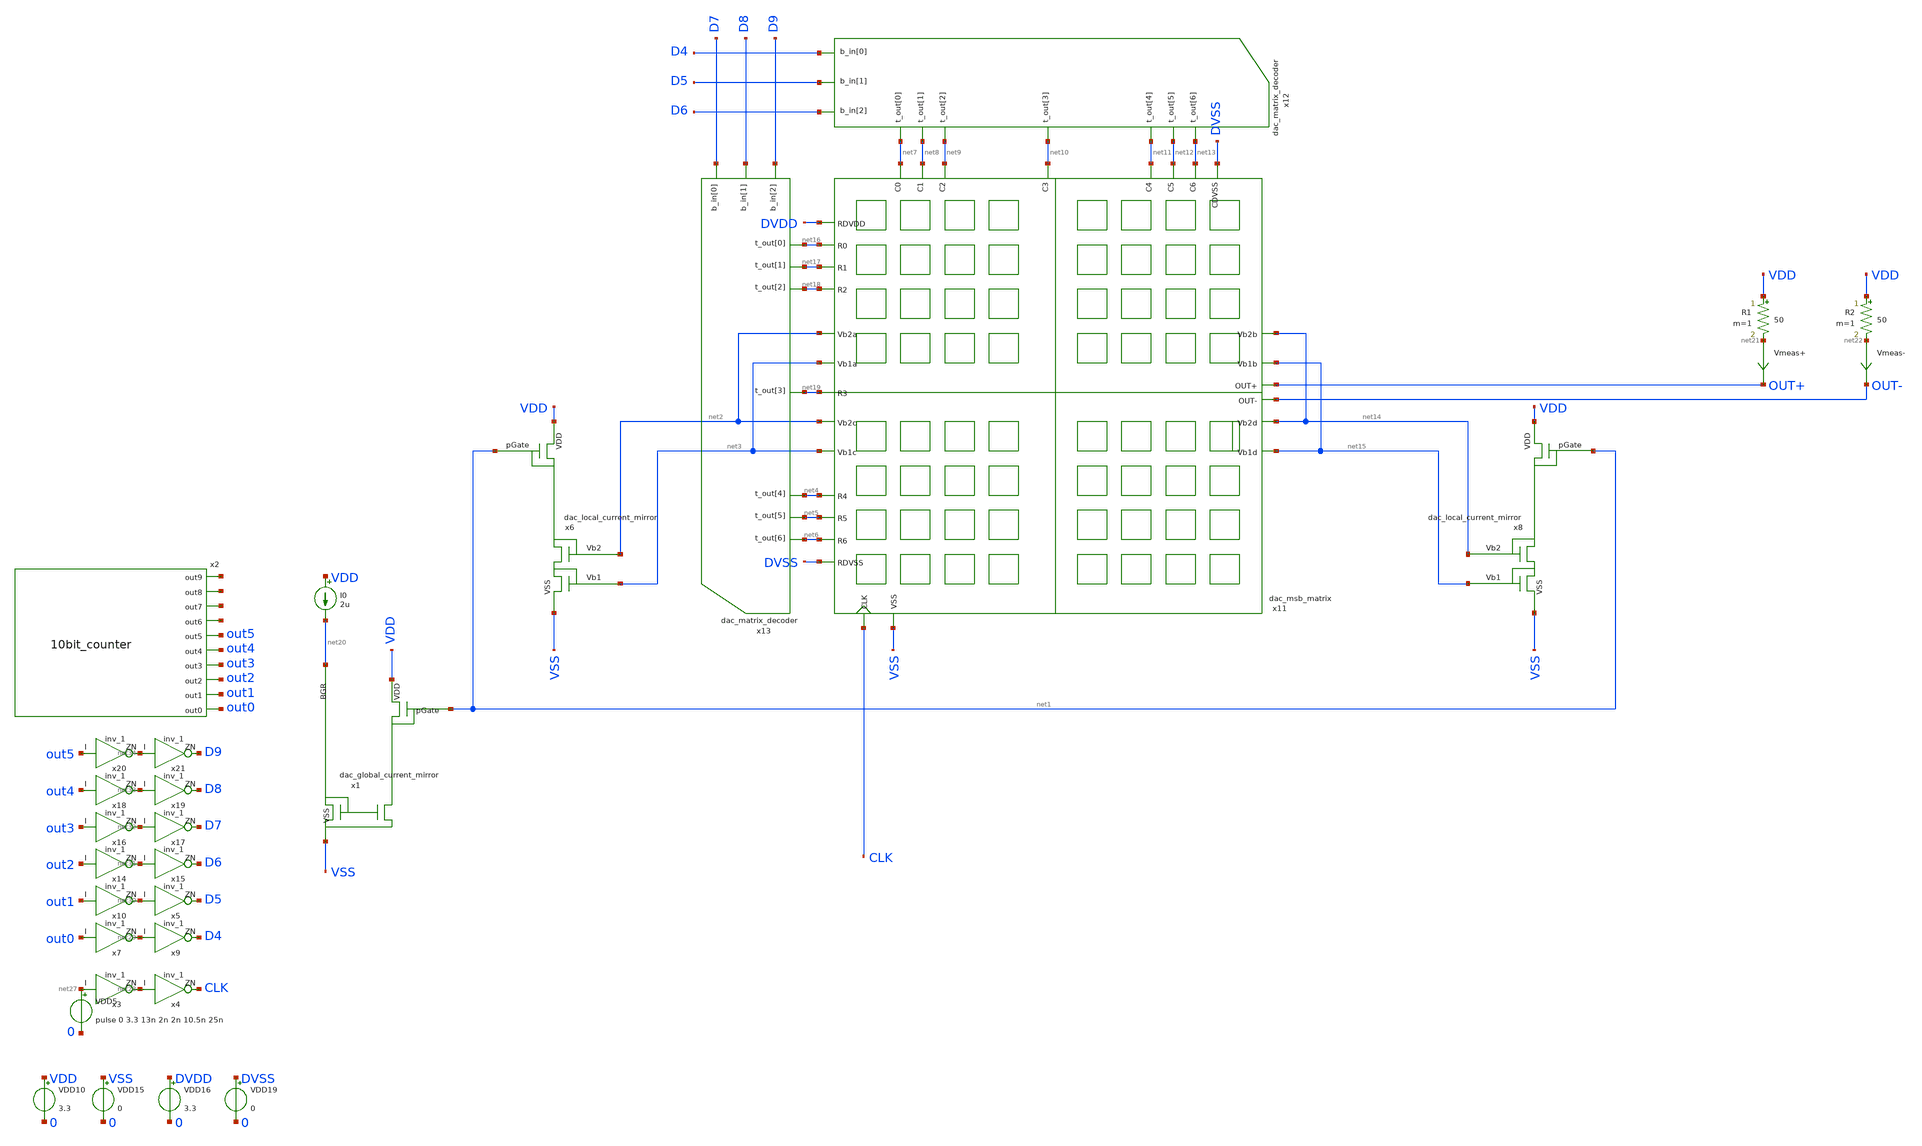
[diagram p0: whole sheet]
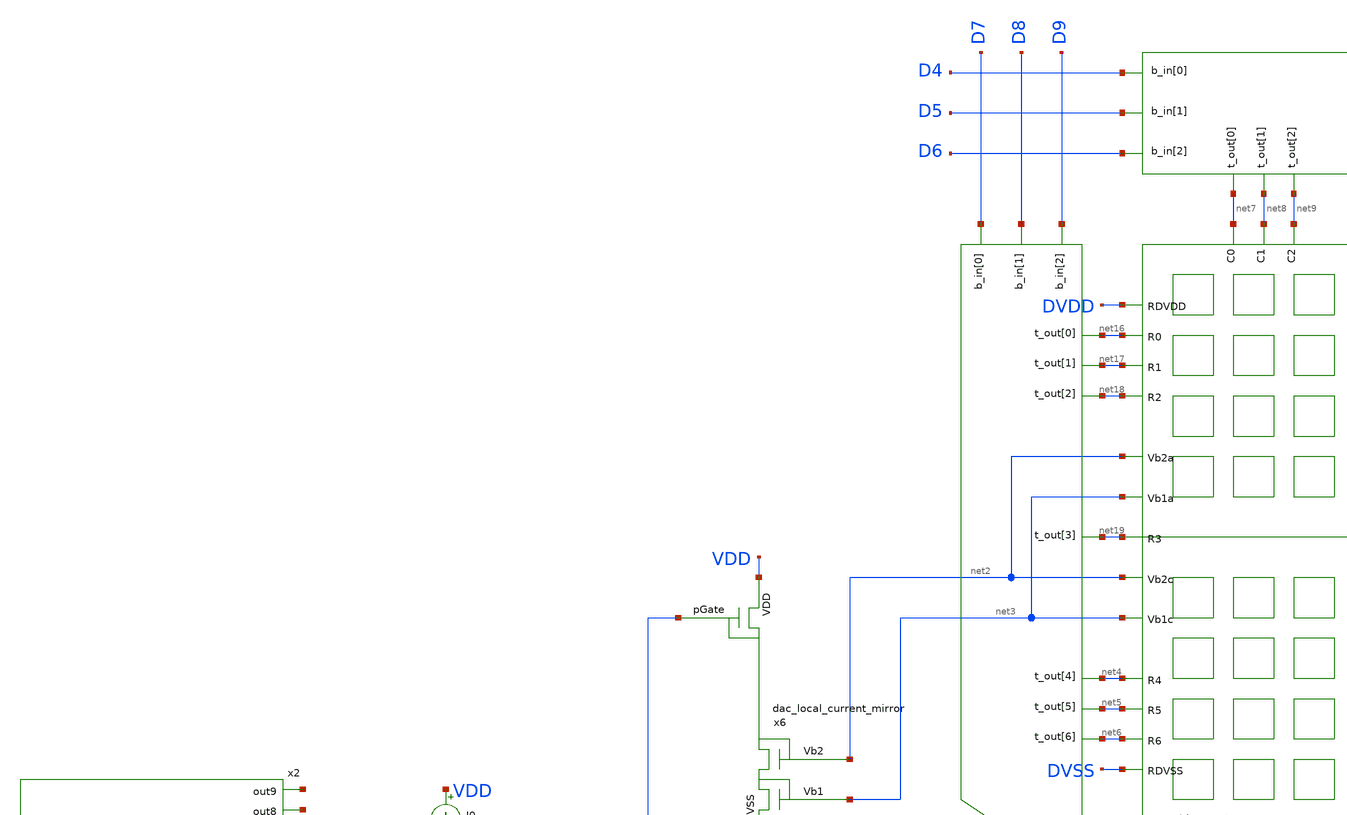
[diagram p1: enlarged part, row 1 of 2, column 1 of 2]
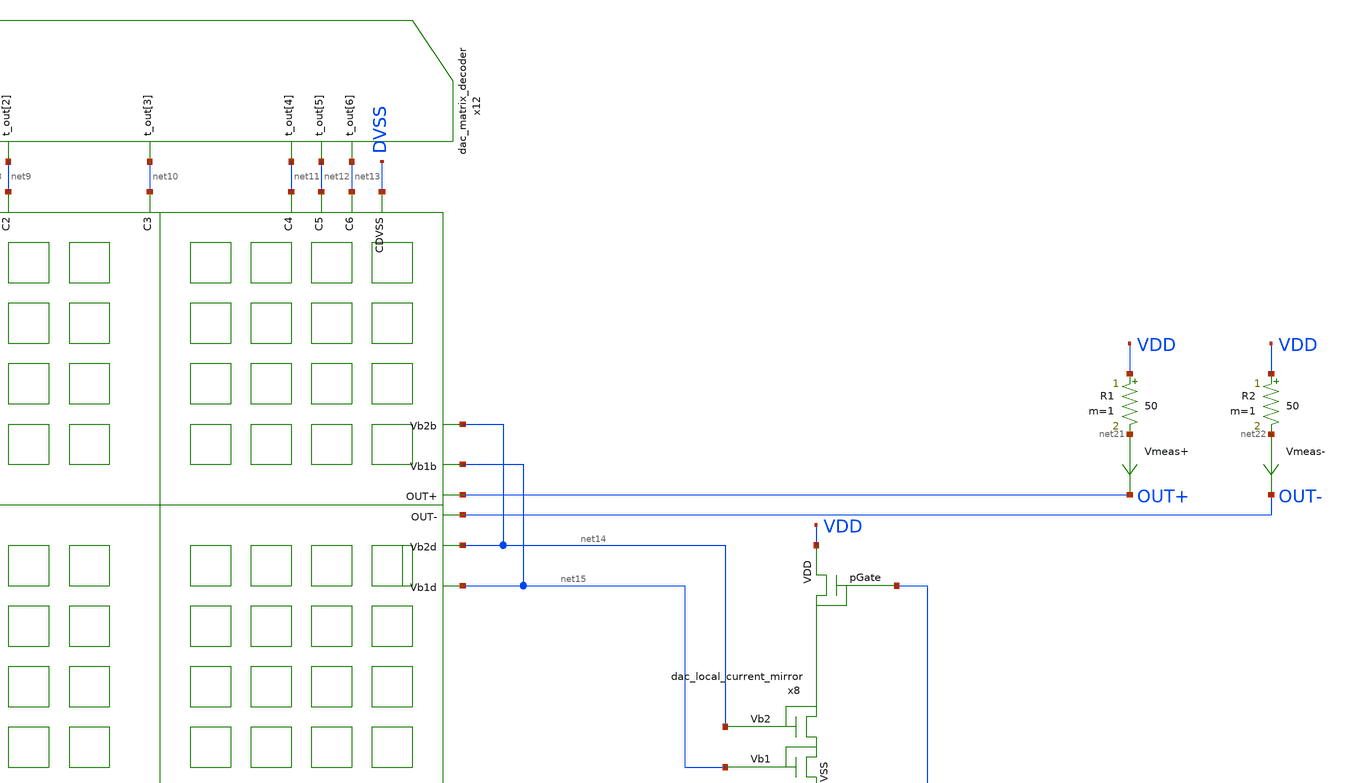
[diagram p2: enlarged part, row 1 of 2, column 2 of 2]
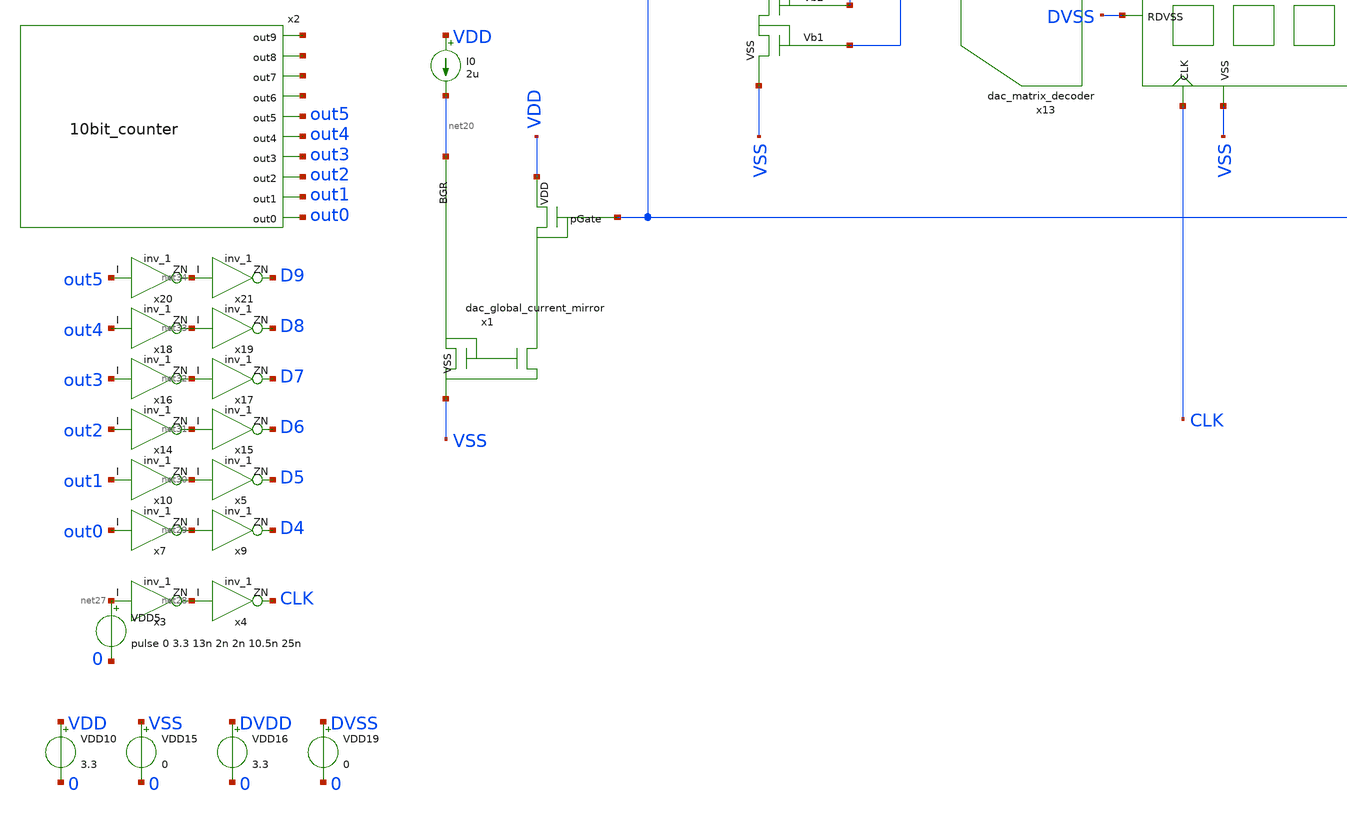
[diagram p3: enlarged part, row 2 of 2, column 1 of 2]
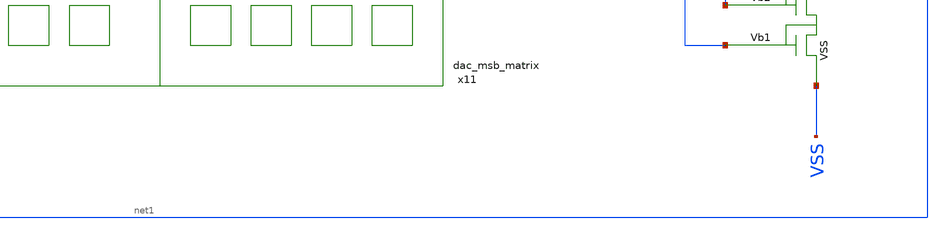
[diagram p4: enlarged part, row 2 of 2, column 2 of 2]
** sch_path: DAC/xschem/tb/tb_dac_msb_matrix.sch
**.subckt tb_dac_msb_matrix
VDD10 VDD 0 3.3
VDD15 VSS 0 0
VDD16 DVDD 0 3.3
VDD19 DVSS 0 0
I0 VDD net20 2u
R1 VDD net21 50 m=1
R2 VDD net22 50 m=1
Vmeas+ net21 OUT+ 0
.save i(vmeas+)
Vmeas- net22 OUT- 0
.save i(vmeas-)
x1 VDD net1 net20 VSS dac_global_current_mirror
x6 VDD net1 net2 net3 VSS dac_local_current_mirror
x8 VDD net1 net14 net15 VSS dac_local_current_mirror
x11 DVDD net16 net17 net18 net19 net4 net5 net6 DVSS net7 net8 net9 net10 net11 net12 net13 DVSS
+ net2 net3 net2 net3 net14 net15 net14 net15 CLK VSS OUT+ OUT- DVDD DVSS dac_msb_matrix
x12 D4 D5 D6 net7 net8 net9 net10 net11 net12 net13 DVDD DVSS dac_matrix_decoder
x13 D7 D8 D9 net16 net17 net18 net19 net4 net5 net6 DVDD DVSS dac_matrix_decoder
x2 out0 out1 out2 out3 out4 out5 net23 net24 net25 net26 10bit_counter
VDD5 net27 0 pulse 0 3.3 13n 2n 2n 10.5n 25n
x3 net27 net28 DVDD DVDD DVSS DVSS gf180mcu_fd_sc_mcu7t5v0__inv_1
x4 net28 CLK DVDD DVDD DVSS DVSS gf180mcu_fd_sc_mcu7t5v0__inv_1
x7 out0 net29 DVDD DVDD DVSS DVSS gf180mcu_fd_sc_mcu7t5v0__inv_1
x9 net29 D4 DVDD DVDD DVSS DVSS gf180mcu_fd_sc_mcu7t5v0__inv_1
x10 out1 net30 DVDD DVDD DVSS DVSS gf180mcu_fd_sc_mcu7t5v0__inv_1
x5 net30 D5 DVDD DVDD DVSS DVSS gf180mcu_fd_sc_mcu7t5v0__inv_1
x14 out2 net31 DVDD DVDD DVSS DVSS gf180mcu_fd_sc_mcu7t5v0__inv_1
x15 net31 D6 DVDD DVDD DVSS DVSS gf180mcu_fd_sc_mcu7t5v0__inv_1
x16 out3 net32 DVDD DVDD DVSS DVSS gf180mcu_fd_sc_mcu7t5v0__inv_1
x17 net32 D7 DVDD DVDD DVSS DVSS gf180mcu_fd_sc_mcu7t5v0__inv_1
x18 out4 net33 DVDD DVDD DVSS DVSS gf180mcu_fd_sc_mcu7t5v0__inv_1
x19 net33 D8 DVDD DVDD DVSS DVSS gf180mcu_fd_sc_mcu7t5v0__inv_1
x20 out5 net34 DVDD DVDD DVSS DVSS gf180mcu_fd_sc_mcu7t5v0__inv_1
x21 net34 D9 DVDD DVDD DVSS DVSS gf180mcu_fd_sc_mcu7t5v0__inv_1
**** begin user architecture code



.control
    tran 1n 1650n
    plot i(Vmeas+) i(Vmeas-)
    write test_dac_msb_matrix.raw
.endc
.save all




.include /home/junbeom/pico/designs/xschem/dac_matrix_decoder.spice
.include $::180MCU_MODELS/design.ngspice
.lib $::180MCU_MODELS/sm141064.ngspice typical
.lib $::180MCU_MODELS/sm141064.ngspice res_typical
.lib $::180MCU_MODELS/sm141064.ngspice moscap_typical
.include $::180MCU_STDCELLS/spice/gf180mcu_fd_sc_mcu7t5v0.spice
*.lib $::180MCU_MODELS/sm141064.ngspice res_statistical

**** end user architecture code
**.ends

* expanding   symbol:  dac_global_current_mirror.sym # of pins=4
** sym_path: DAC/xschem/dac_global_current_mirror.sym
** sch_path: DAC/xschem/dac_global_current_mirror.sch
.subckt dac_global_current_mirror VDD pGate BGR VSS
*.ipin BGR
*.ipin VDD
*.opin pGate
*.ipin VSS
XM1 pGate pGate VDD VDD pfet_03v3 L=1u W=1u nf=1 ad='int((nf+1)/2) * W/nf * 0.18u' as='int((nf+2)/2) * W/nf * 0.18u'
+ pd='2*int((nf+1)/2) * (W/nf + 0.18u)' ps='2*int((nf+2)/2) * (W/nf + 0.18u)' nrd='0.18u / W' nrs='0.18u / W'
+ sa=0 sb=0 sd=0 m=1
XMN1 BGR BGR VSS VSS nfet_03v3 L=4u W=1u nf=4 ad='int((nf+1)/2) * W/nf * 0.18u' as='int((nf+2)/2) * W/nf * 0.18u'
+ pd='2*int((nf+1)/2) * (W/nf + 0.18u)' ps='2*int((nf+2)/2) * (W/nf + 0.18u)' nrd='0.18u / W' nrs='0.18u / W'
+ sa=0 sb=0 sd=0 m=1
XMN2 pGate BGR VSS VSS nfet_03v3 L=4u W=1u nf=4 ad='int((nf+1)/2) * W/nf * 0.18u' as='int((nf+2)/2) * W/nf * 0.18u'
+ pd='2*int((nf+1)/2) * (W/nf + 0.18u)' ps='2*int((nf+2)/2) * (W/nf + 0.18u)' nrd='0.18u / W' nrs='0.18u / W'
+ sa=0 sb=0 sd=0 m=1
.ends


* expanding   symbol:  dac_local_current_mirror.sym # of pins=5
** sym_path: DAC/xschem/dac_local_current_mirror.sym
** sch_path: DAC/xschem/dac_local_current_mirror.sch
.subckt dac_local_current_mirror VDD pGate Vb2 Vb1 VSS
*.ipin VSS
*.opin Vb2
*.opin Vb1
*.ipin VDD
*.ipin pGate
XM2 Vb2 pGate VDD VDD pfet_03v3 L=1u W=5u nf=5 ad='int((nf+1)/2) * W/nf * 0.18u' as='int((nf+2)/2) * W/nf * 0.18u'
+ pd='2*int((nf+1)/2) * (W/nf + 0.18u)' ps='2*int((nf+2)/2) * (W/nf + 0.18u)' nrd='0.18u / W' nrs='0.18u / W'
+ sa=0 sb=0 sd=0 m=1
XM5 Vb2 Vb2 Vb1 VSS nfet_03v3 L=1u W=4u nf=4 ad='int((nf+1)/2) * W/nf * 0.18u' as='int((nf+2)/2) * W/nf * 0.18u'
+ pd='2*int((nf+1)/2) * (W/nf + 0.18u)' ps='2*int((nf+2)/2) * (W/nf + 0.18u)' nrd='0.18u / W' nrs='0.18u / W'
+ sa=0 sb=0 sd=0 m=1
XM6 Vb1 Vb1 VSS VSS nfet_03v3 L=1u W=4u nf=4 ad='int((nf+1)/2) * W/nf * 0.18u' as='int((nf+2)/2) * W/nf * 0.18u'
+ pd='2*int((nf+1)/2) * (W/nf + 0.18u)' ps='2*int((nf+2)/2) * (W/nf + 0.18u)' nrd='0.18u / W' nrs='0.18u / W'
+ sa=0 sb=0 sd=0 m=1
.ends


* expanding   symbol:  dac_msb_matrix.sym # of pins=29
** sym_path: DAC/xschem/dac_msb_matrix.sym
** sch_path: DAC/xschem/dac_msb_matrix.sch
.subckt dac_msb_matrix RDVDD R0 R1 R2 R3 R4 R5 R6 RDVSS C0 C1 C2 C3 C4 C5 C6 CDVSS Vb2a Vb1a Vb2c
+ Vb1c Vb2b Vb1b Vb2d Vb1d CLK VSS OUT+ OUT- DVDD DVSS
*.ipin R0
*.ipin R1
*.ipin R2
*.ipin R3
*.ipin R4
*.ipin R5
*.ipin R6
*.ipin C0
*.ipin C1
*.ipin C2
*.ipin C3
*.ipin C4
*.ipin C5
*.ipin C6
*.ipin VSS
*.ipin Vb2a
*.ipin Vb1a
*.ipin Vb2b
*.ipin Vb1b
*.ipin Vb2c
*.ipin Vb1c
*.ipin Vb2d
*.ipin Vb1d
*.opin OUT+
*.opin OUT-
*.ipin CLK
*.ipin RDVDD
*.ipin RDVSS
*.ipin CDVSS
x1 R3 R4 R4 R5 R5 R6 R6 RDVSS C0 C1 C2 C3 CLK Vb2c Vb1c VSS OUT+ OUT- DVDD DVSS
+ dac_msb_quarter_matrix
x3 R3 R4 R4 R5 R5 R6 R6 RDVSS C4 C5 C6 CDVSS CLK Vb2d Vb1d VSS OUT+ OUT- DVDD DVSS
+ dac_msb_quarter_matrix
x4 RDVDD R0 R0 R1 R1 R2 R2 R3 C4 C5 C6 CDVSS CLK Vb2b Vb1b VSS OUT+ OUT- DVDD DVSS
+ dac_msb_quarter_matrix
x5 RDVDD R0 R0 R1 R1 R2 R2 R3 C0 C1 C2 C3 CLK Vb2a Vb1a VSS OUT+ OUT- DVDD DVSS
+ dac_msb_quarter_matrix
.ends


* expanding   symbol:  10bit_counter.sym # of pins=10
** sym_path: DAC/xschem/10bit_counter.sym
.include /home/junbeom/pico/designs/xschem/10bit_Counter.sp

* expanding   symbol:  dac_msb_quarter_matrix.sym # of pins=18
** sym_path: DAC/xschem/dac_msb_quarter_matrix.sym
** sch_path: DAC/xschem/dac_msb_quarter_matrix.sch
.subckt dac_msb_quarter_matrix R0 R1 R2 R3 R4 R5 R6 R7 C0 C1 C2 C3 CLK Vb2 Vb1 VSS OUT+ OUT- DVDD
+ DVSS
*.ipin CLK
*.ipin R0
*.ipin R1
*.ipin R2
*.ipin R3
*.ipin R4
*.ipin R5
*.ipin R6
*.ipin R7
*.ipin C0
*.ipin C1
*.ipin C2
*.ipin C3
*.ipin VSS
*.ipin Vb2
*.ipin Vb1
*.opin OUT+
*.opin OUT-
x13 C0 R6 R7 CLK Vb2 Vb1 VSS OUT+ OUT- DVDD DVSS dac_msb_cell
x1 C1 R6 R7 CLK Vb2 Vb1 VSS OUT+ OUT- DVDD DVSS dac_msb_cell
x3 C2 R6 R7 CLK Vb2 Vb1 VSS OUT+ OUT- DVDD DVSS dac_msb_cell
x5 C3 R6 R7 CLK Vb2 Vb1 VSS OUT+ OUT- DVDD DVSS dac_msb_cell
x2 C0 R4 R5 CLK Vb2 Vb1 VSS OUT+ OUT- DVDD DVSS dac_msb_cell
x4 C1 R4 R5 CLK Vb2 Vb1 VSS OUT+ OUT- DVDD DVSS dac_msb_cell
x6 C2 R4 R5 CLK Vb2 Vb1 VSS OUT+ OUT- DVDD DVSS dac_msb_cell
x7 C3 R4 R5 CLK Vb2 Vb1 VSS OUT+ OUT- DVDD DVSS dac_msb_cell
x8 C0 R2 R3 CLK Vb2 Vb1 VSS OUT+ OUT- DVDD DVSS dac_msb_cell
x9 C1 R2 R3 CLK Vb2 Vb1 VSS OUT+ OUT- DVDD DVSS dac_msb_cell
x10 C2 R2 R3 CLK Vb2 Vb1 VSS OUT+ OUT- DVDD DVSS dac_msb_cell
x11 C3 R2 R3 CLK Vb2 Vb1 VSS OUT+ OUT- DVDD DVSS dac_msb_cell
x12 C0 R0 R1 CLK Vb2 Vb1 VSS OUT+ OUT- DVDD DVSS dac_msb_cell
x14 C1 R0 R1 CLK Vb2 Vb1 VSS OUT+ OUT- DVDD DVSS dac_msb_cell
x15 C2 R0 R1 CLK Vb2 Vb1 VSS OUT+ OUT- DVDD DVSS dac_msb_cell
x16 C3 R0 R1 CLK Vb2 Vb1 VSS OUT+ OUT- DVDD DVSS dac_msb_cell
.ends


* expanding   symbol:  dac_msb_cell.sym # of pins=9
** sym_path: DAC/xschem/dac_msb_cell.sym
** sch_path: DAC/xschem/dac_msb_cell.sch
.subckt dac_msb_cell Cj Ri Rk CLK Vb2 Vb1 VSS OUT+ OUT- DVDD DVSS
*.ipin Cj
*.ipin Rk
*.ipin Ri
*.ipin CLK
*.ipin Vb2
*.ipin Vb1
*.ipin VSS
*.opin OUT+
*.opin OUT-
x2 net4 CLK net1 DVDD DVDD DVSS DVSS gf180mcu_fd_sc_mcu7t5v0__dffq_1
x3 net1 net2 DVDD DVDD DVSS DVSS gf180mcu_fd_sc_mcu7t5v0__inv_1
x6 Cj Ri net3 DVDD DVDD DVSS DVSS gf180mcu_fd_sc_mcu7t5v0__and2_1
x4 net3 Rk net4 DVDD DVDD DVSS DVSS gf180mcu_fd_sc_mcu7t5v0__or2_1
x1 OUT+ OUT- net2 net1 Vb2 Vb1 VSS dac_msb_analog
.ends


* expanding   symbol:  dac_msb_analog.sym # of pins=7
** sym_path: DAC/xschem/dac_msb_analog.sym
** sch_path: DAC/xschem/dac_msb_analog.sch
.subckt dac_msb_analog OUT+ OUT- Q- Q+ Vb2 Vb1 VSS
*.ipin Q-
*.ipin Q+
*.ipin Vb1
*.ipin Vb2
*.opin OUT+
*.opin OUT-
*.ipin VSS
XM26 net1 Vb2 net2 VSS nfet_03v3 L=0.5u W=32u nf=16 ad='int((nf+1)/2) * W/nf * 0.18u' as='int((nf+2)/2) * W/nf * 0.18u'
+ pd='2*int((nf+1)/2) * (W/nf + 0.18u)' ps='2*int((nf+2)/2) * (W/nf + 0.18u)' nrd='0.18u / W' nrs='0.18u / W'
+ sa=0 sb=0 sd=0 m=1
XM27 net2 Vb1 VSS VSS nfet_03v3 L=0.5u W=32u nf=16 ad='int((nf+1)/2) * W/nf * 0.18u' as='int((nf+2)/2) * W/nf * 0.18u'
+ pd='2*int((nf+1)/2) * (W/nf + 0.18u)' ps='2*int((nf+2)/2) * (W/nf + 0.18u)' nrd='0.18u / W' nrs='0.18u / W'
+ sa=0 sb=0 sd=0 m=1
XM30 OUT+ Q+ net1 VSS nfet_03v3 L=0.5u W=16u nf=8 ad='int((nf+1)/2) * W/nf * 0.18u' as='int((nf+2)/2) * W/nf * 0.18u'
+ pd='2*int((nf+1)/2) * (W/nf + 0.18u)' ps='2*int((nf+2)/2) * (W/nf + 0.18u)' nrd='0.18u / W' nrs='0.18u / W'
+ sa=0 sb=0 sd=0 m=1
XM31 OUT- Q- net1 VSS nfet_03v3 L=0.5u W=16u nf=8 ad='int((nf+1)/2) * W/nf * 0.18u' as='int((nf+2)/2) * W/nf * 0.18u'
+ pd='2*int((nf+1)/2) * (W/nf + 0.18u)' ps='2*int((nf+2)/2) * (W/nf + 0.18u)' nrd='0.18u / W' nrs='0.18u / W'
+ sa=0 sb=0 sd=0 m=1
.ends

.end
